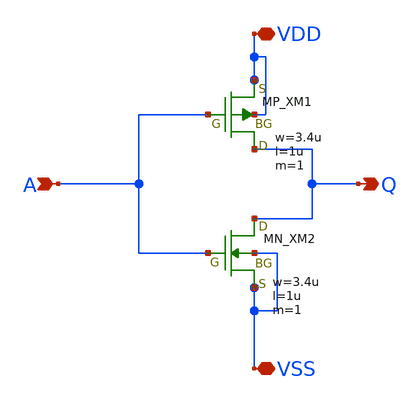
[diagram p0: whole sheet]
** sch_path: schematic/20250924_OSS_Workshop/Qdai/inverter_MUX_01/inv_kyo.sch
**.subckt inv_kyo A VDD Q VSS
*.ipin A
*.iopin VDD
*.opin Q
*.iopin VSS
XM2 Q A VSS VSS NMOS w=3.4u l=1u as=0 ad=0 ps=0 pd=0 nrd=0 nrs=0 m=1
XM1 Q A VDD VDD PMOS w=3.4u l=1u as=0 ad=0 ps=0 pd=0 nrd=0 nrs=0 m=1
**.ends
.end
